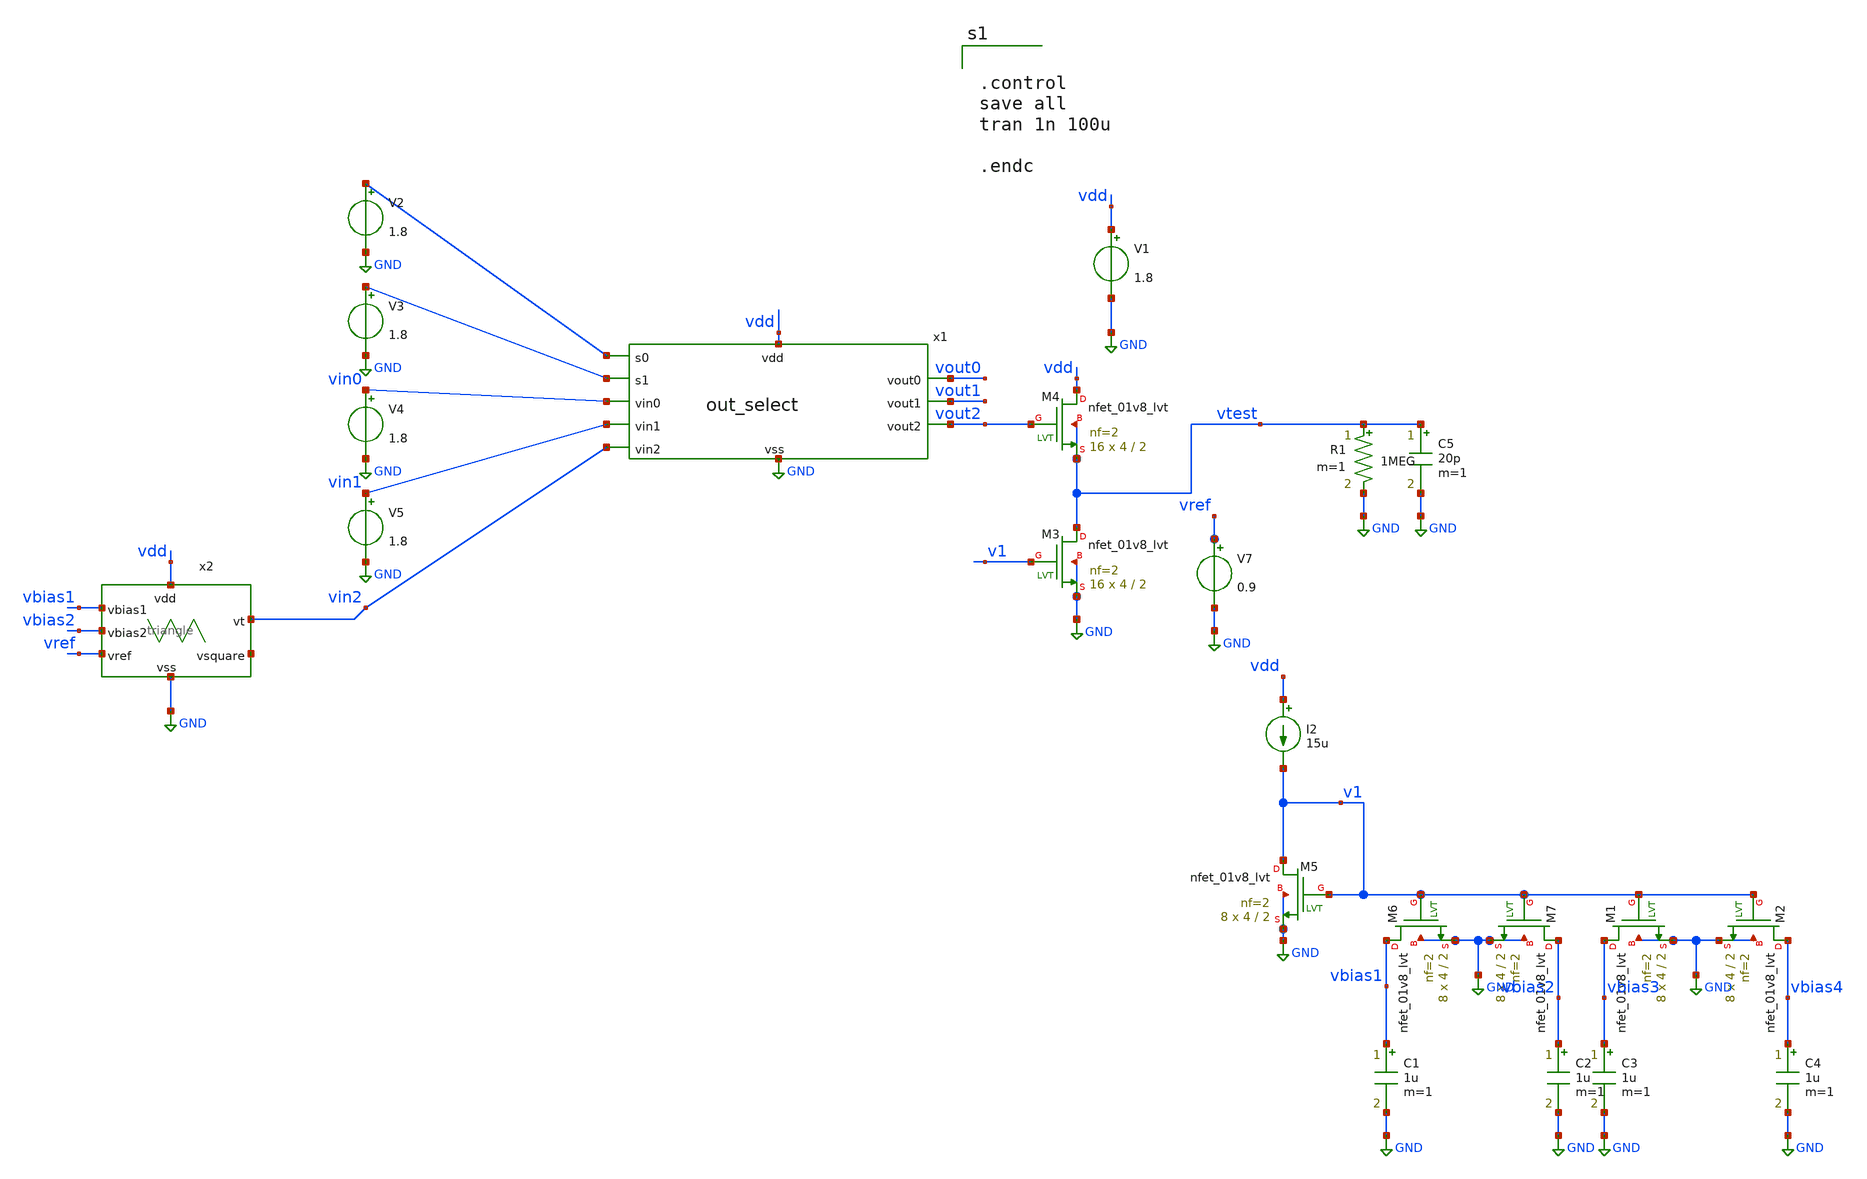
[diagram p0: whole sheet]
** sch_path: xschem/src/output_select/out_select_tb.sch
**.subckt out_select_tb
x1 vdd vin0 vout0 GND net1 vin1 vout1 net2 vin2 vout2 out_select
V1 vdd GND 1.8
V2 net1 GND 1.8
V3 net2 GND 1.8
V4 vin0 GND 1.8
V5 vin1 GND 1.8
V7 vref GND 0.9
I2 vdd v1 15u
XM5 v1 v1 GND GND sky130_fd_pr__nfet_01v8_lvt L=2 W=4 nf=2 ad='int((nf+1)/2) * W/nf * 0.29' as='int((nf+2)/2) * W/nf * 0.29'
+ pd='2*int((nf+1)/2) * (W/nf + 0.29)' ps='2*int((nf+2)/2) * (W/nf + 0.29)' nrd='0.29 / W' nrs='0.29 / W'
+ sa=0 sb=0 sd=0 mult=8 m=8
XM6 vbias1 v1 GND GND sky130_fd_pr__nfet_01v8_lvt L=2 W=4 nf=2 ad='int((nf+1)/2) * W/nf * 0.29' as='int((nf+2)/2) * W/nf * 0.29'
+ pd='2*int((nf+1)/2) * (W/nf + 0.29)' ps='2*int((nf+2)/2) * (W/nf + 0.29)' nrd='0.29 / W' nrs='0.29 / W'
+ sa=0 sb=0 sd=0 mult=8 m=8
XM7 vbias2 v1 GND GND sky130_fd_pr__nfet_01v8_lvt L=2 W=4 nf=2 ad='int((nf+1)/2) * W/nf * 0.29' as='int((nf+2)/2) * W/nf * 0.29'
+ pd='2*int((nf+1)/2) * (W/nf + 0.29)' ps='2*int((nf+2)/2) * (W/nf + 0.29)' nrd='0.29 / W' nrs='0.29 / W'
+ sa=0 sb=0 sd=0 mult=8 m=8
XM1 vbias3 v1 GND GND sky130_fd_pr__nfet_01v8_lvt L=2 W=4 nf=2 ad='int((nf+1)/2) * W/nf * 0.29' as='int((nf+2)/2) * W/nf * 0.29'
+ pd='2*int((nf+1)/2) * (W/nf + 0.29)' ps='2*int((nf+2)/2) * (W/nf + 0.29)' nrd='0.29 / W' nrs='0.29 / W'
+ sa=0 sb=0 sd=0 mult=8 m=8
XM2 vbias4 v1 GND GND sky130_fd_pr__nfet_01v8_lvt L=2 W=4 nf=2 ad='int((nf+1)/2) * W/nf * 0.29' as='int((nf+2)/2) * W/nf * 0.29'
+ pd='2*int((nf+1)/2) * (W/nf + 0.29)' ps='2*int((nf+2)/2) * (W/nf + 0.29)' nrd='0.29 / W' nrs='0.29 / W'
+ sa=0 sb=0 sd=0 mult=8 m=8
C1 vbias1 GND 1u m=1
C2 vbias2 GND 1u m=1
C3 vbias3 GND 1u m=1
C4 vbias4 GND 1u m=1
x2 vdd vbias1 vbias2 vref GND net3 vin2 triangle
C5 vtest GND 20p m=1
XM4 vdd vout2 vtest vtest sky130_fd_pr__nfet_01v8_lvt L=2 W=4 nf=2 ad='int((nf+1)/2) * W/nf * 0.29' as='int((nf+2)/2) * W/nf * 0.29'
+ pd='2*int((nf+1)/2) * (W/nf + 0.29)' ps='2*int((nf+2)/2) * (W/nf + 0.29)' nrd='0.29 / W' nrs='0.29 / W'
+ sa=0 sb=0 sd=0 mult=16 m=16
XM3 vtest v1 GND GND sky130_fd_pr__nfet_01v8_lvt L=2 W=4 nf=2 ad='int((nf+1)/2) * W/nf * 0.29' as='int((nf+2)/2) * W/nf * 0.29'
+ pd='2*int((nf+1)/2) * (W/nf + 0.29)' ps='2*int((nf+2)/2) * (W/nf + 0.29)' nrd='0.29 / W' nrs='0.29 / W'
+ sa=0 sb=0 sd=0 mult=16 m=16
R1 vtest GND 1MEG m=1
**** begin user architecture code

.include /home/eda/pdk/skywater-pdk/libraries/sky130_fd_pr_ngspice/latest/models/corners/tt.spice
.include /home/eda/magic/class_d_audio_amplifier/Class_D/Class_D_post.spice

* Resistor$::SKYWATER_MODELS/Capacitor
.include $::SKYWATER_MODELS/models/r+c/res_typical__cap_typical.spice
.include $::SKYWATER_MODELS/models/r+c/res_typical__cap_typical__lin.spice
* Special cells
.include $::SKYWATER_MODELS/models/corners/tt/specialized_cells.spice




.control
save all
tran 1n 100u

.endc




**** end user architecture code
**.ends

* expanding   symbol:  src/output_select/out_select.sym # of pins=10
** sym_path: xschem/src/output_select/out_select.sym
** sch_path: xschem/src/output_select/out_select.sch
.subckt out_select vdd vin0 vout0 vss s0 vin1 vout1 s1 vin2 vout2
*.ipin vin0
*.opin vout0
*.ipin vin1
*.opin vout1
*.ipin vin2
*.opin vout2
*.iopin vdd
*.iopin vss
*.ipin s0
*.ipin s1
x4 vdd sel0 net1 s1 vss nand
x5 vdd sel1 s0 net2 net4 nand
x6 vdd sel2 s0 s1 vss nand
x8 vdd s1 net2 vss inverter
x9 vdd s0 net1 vss inverter
x7 vdd sel2 net3 vss inverter
x10 vdd sel1 net7 net5 inverter
x11 vdd sel0 net6 vss inverter
XM1 vin0 net6 vout0 vout0 sky130_fd_pr__nfet_01v8 L=0.15 W=1 nf=1 ad='int((nf+1)/2) * W/nf * 0.29' as='int((nf+2)/2) * W/nf * 0.29'
+ pd='2*int((nf+1)/2) * (W/nf + 0.29)' ps='2*int((nf+2)/2) * (W/nf + 0.29)' nrd='0.29 / W' nrs='0.29 / W'
+ sa=0 sb=0 sd=0 mult=1 m=1
XM2 vin0 sel0 vout0 vout0 sky130_fd_pr__pfet_01v8 L=0.15 W=1 nf=1 ad='int((nf+1)/2) * W/nf * 0.29' as='int((nf+2)/2) * W/nf * 0.29'
+ pd='2*int((nf+1)/2) * (W/nf + 0.29)' ps='2*int((nf+2)/2) * (W/nf + 0.29)' nrd='0.29 / W' nrs='0.29 / W'
+ sa=0 sb=0 sd=0 mult=1 m=1
XM3 vin1 net7 vout1 vout1 sky130_fd_pr__nfet_01v8 L=0.15 W=1 nf=1 ad='int((nf+1)/2) * W/nf * 0.29' as='int((nf+2)/2) * W/nf * 0.29'
+ pd='2*int((nf+1)/2) * (W/nf + 0.29)' ps='2*int((nf+2)/2) * (W/nf + 0.29)' nrd='0.29 / W' nrs='0.29 / W'
+ sa=0 sb=0 sd=0 mult=1 m=1
XM4 vin1 sel1 vout1 vout1 sky130_fd_pr__pfet_01v8 L=0.15 W=1 nf=1 ad='int((nf+1)/2) * W/nf * 0.29' as='int((nf+2)/2) * W/nf * 0.29'
+ pd='2*int((nf+1)/2) * (W/nf + 0.29)' ps='2*int((nf+2)/2) * (W/nf + 0.29)' nrd='0.29 / W' nrs='0.29 / W'
+ sa=0 sb=0 sd=0 mult=1 m=1
XM5 vin2 net3 vout2 vout2 sky130_fd_pr__nfet_01v8 L=0.15 W=1 nf=1 ad='int((nf+1)/2) * W/nf * 0.29' as='int((nf+2)/2) * W/nf * 0.29'
+ pd='2*int((nf+1)/2) * (W/nf + 0.29)' ps='2*int((nf+2)/2) * (W/nf + 0.29)' nrd='0.29 / W' nrs='0.29 / W'
+ sa=0 sb=0 sd=0 mult=1 m=1
XM6 vin2 sel2 vout2 vout2 sky130_fd_pr__pfet_01v8 L=0.15 W=1 nf=1 ad='int((nf+1)/2) * W/nf * 0.29' as='int((nf+2)/2) * W/nf * 0.29'
+ pd='2*int((nf+1)/2) * (W/nf + 0.29)' ps='2*int((nf+2)/2) * (W/nf + 0.29)' nrd='0.29 / W' nrs='0.29 / W'
+ sa=0 sb=0 sd=0 mult=1 m=1
.ends


* expanding   symbol:  src/triangle/triangle.sym # of pins=7
** sym_path: xschem/src/triangle/triangle.sym
** sch_path: xschem/src/triangle/triangle.sch
.subckt triangle vdd vbias1 vbias2 vref vss vsquare vt
*.iopin vdd
*.ipin vbias1
*.opin vt
*.ipin vref
*.opin vsquare
*.iopin vss
*.ipin vbias2
XR3 vsquare vi vss sky130_fd_pr__res_xhigh_po L=32 mult=1 m=1
XR1 vt vcmp vss sky130_fd_pr__res_xhigh_po L=4 mult=1 m=1
XR2 vcmp vsquare vss sky130_fd_pr__res_xhigh_po L=9 mult=1 m=1
x1 vdd vref vi vbias1 vss vt OTA_tri
x2 vdd vcmp vref vbias2 vss vsquare OTA
XC1 vi vt sky130_fd_pr__cap_mim_m3_1 W=15 L=15 MF=8 m=8
.ends


* expanding   symbol:  src/nand/nand.sym # of pins=5
** sym_path: xschem/src/nand/nand.sym
** sch_path: xschem/src/nand/nand.sch
.subckt nand vdd out A B vss
*.ipin A
*.ipin B
*.opin out
*.iopin vdd
*.iopin vss
XM1 out A net1 vss sky130_fd_pr__nfet_01v8 L=0.15 W=2 nf=1 ad='int((nf+1)/2) * W/nf * 0.29' as='int((nf+2)/2) * W/nf * 0.29'
+ pd='2*int((nf+1)/2) * (W/nf + 0.29)' ps='2*int((nf+2)/2) * (W/nf + 0.29)' nrd='0.29 / W' nrs='0.29 / W'
+ sa=0 sb=0 sd=0 mult=1 m=1
XM2 out A vdd vdd sky130_fd_pr__pfet_01v8 L=0.15 W=2 nf=1 ad='int((nf+1)/2) * W/nf * 0.29' as='int((nf+2)/2) * W/nf * 0.29'
+ pd='2*int((nf+1)/2) * (W/nf + 0.29)' ps='2*int((nf+2)/2) * (W/nf + 0.29)' nrd='0.29 / W' nrs='0.29 / W'
+ sa=0 sb=0 sd=0 mult=1 m=1
XM3 net1 B vss vss sky130_fd_pr__nfet_01v8 L=0.15 W=2 nf=1 ad='int((nf+1)/2) * W/nf * 0.29' as='int((nf+2)/2) * W/nf * 0.29'
+ pd='2*int((nf+1)/2) * (W/nf + 0.29)' ps='2*int((nf+2)/2) * (W/nf + 0.29)' nrd='0.29 / W' nrs='0.29 / W'
+ sa=0 sb=0 sd=0 mult=1 m=1
XM4 out B vdd vdd sky130_fd_pr__pfet_01v8 L=0.15 W=2 nf=1 ad='int((nf+1)/2) * W/nf * 0.29' as='int((nf+2)/2) * W/nf * 0.29'
+ pd='2*int((nf+1)/2) * (W/nf + 0.29)' ps='2*int((nf+2)/2) * (W/nf + 0.29)' nrd='0.29 / W' nrs='0.29 / W'
+ sa=0 sb=0 sd=0 mult=1 m=1
.ends


* expanding   symbol:  src/inverter/inverter.sym # of pins=4
** sym_path: xschem/src/inverter/inverter.sym
** sch_path: xschem/src/inverter/inverter.sch
.subckt inverter vdd A B vss
*.iopin vdd
*.iopin vss
*.ipin A
*.opin B
XM3 B A vss vss sky130_fd_pr__nfet_01v8 L=0.15 W=1 nf=1 ad='int((nf+1)/2) * W/nf * 0.29' as='int((nf+2)/2) * W/nf * 0.29'
+ pd='2*int((nf+1)/2) * (W/nf + 0.29)' ps='2*int((nf+2)/2) * (W/nf + 0.29)' nrd='0.29 / W' nrs='0.29 / W'
+ sa=0 sb=0 sd=0 mult=1 m=1
XM1 B A vdd vdd sky130_fd_pr__pfet_01v8 L=0.15 W=2 nf=1 ad='int((nf+1)/2) * W/nf * 0.29' as='int((nf+2)/2) * W/nf * 0.29'
+ pd='2*int((nf+1)/2) * (W/nf + 0.29)' ps='2*int((nf+2)/2) * (W/nf + 0.29)' nrd='0.29 / W' nrs='0.29 / W'
+ sa=0 sb=0 sd=0 mult=1 m=1
.ends


* expanding   symbol:  src/OTA_tri/OTA_tri.sym # of pins=6
** sym_path: xschem/src/OTA_tri/OTA_tri.sym
** sch_path: xschem/src/OTA_tri/OTA_tri.sch
.subckt OTA_tri vdd vp vn vbias vss vout
*.ipin vp
*.ipin vn
*.ipin vbias
*.iopin vss
*.iopin vdd
*.opin vout
XM1 v1 vp vc vc sky130_fd_pr__pfet_01v8_lvt L=1 W=4 nf=1 ad='int((nf+1)/2) * W/nf * 0.29' as='int((nf+2)/2) * W/nf * 0.29'
+ pd='2*int((nf+1)/2) * (W/nf + 0.29)' ps='2*int((nf+2)/2) * (W/nf + 0.29)' nrd='0.29 / W' nrs='0.29 / W'
+ sa=0 sb=0 sd=0 mult=16 m=16
XM2 vf vn vc vc sky130_fd_pr__pfet_01v8_lvt L=1 W=4 nf=1 ad='int((nf+1)/2) * W/nf * 0.29' as='int((nf+2)/2) * W/nf * 0.29'
+ pd='2*int((nf+1)/2) * (W/nf + 0.29)' ps='2*int((nf+2)/2) * (W/nf + 0.29)' nrd='0.29 / W' nrs='0.29 / W'
+ sa=0 sb=0 sd=0 mult=16 m=16
XM3 vc vbias vdd vdd sky130_fd_pr__pfet_01v8_lvt L=1 W=2 nf=2 ad='int((nf+1)/2) * W/nf * 0.29' as='int((nf+2)/2) * W/nf * 0.29'
+ pd='2*int((nf+1)/2) * (W/nf + 0.29)' ps='2*int((nf+2)/2) * (W/nf + 0.29)' nrd='0.29 / W' nrs='0.29 / W'
+ sa=0 sb=0 sd=0 mult=24 m=24
XM4 v1 vf vss vss sky130_fd_pr__nfet_01v8_lvt L=1 W=1 nf=1 ad='int((nf+1)/2) * W/nf * 0.29' as='int((nf+2)/2) * W/nf * 0.29'
+ pd='2*int((nf+1)/2) * (W/nf + 0.29)' ps='2*int((nf+2)/2) * (W/nf + 0.29)' nrd='0.29 / W' nrs='0.29 / W'
+ sa=0 sb=0 sd=0 mult=16 m=16
XM5 vf vf vss vss sky130_fd_pr__nfet_01v8_lvt L=1 W=1 nf=1 ad='int((nf+1)/2) * W/nf * 0.29' as='int((nf+2)/2) * W/nf * 0.29'
+ pd='2*int((nf+1)/2) * (W/nf + 0.29)' ps='2*int((nf+2)/2) * (W/nf + 0.29)' nrd='0.29 / W' nrs='0.29 / W'
+ sa=0 sb=0 sd=0 mult=16 m=16
XM6 vbias vbias vdd vdd sky130_fd_pr__pfet_01v8_lvt L=1 W=2 nf=2 ad='int((nf+1)/2) * W/nf * 0.29' as='int((nf+2)/2) * W/nf * 0.29'
+ pd='2*int((nf+1)/2) * (W/nf + 0.29)' ps='2*int((nf+2)/2) * (W/nf + 0.29)' nrd='0.29 / W' nrs='0.29 / W'
+ sa=0 sb=0 sd=0 mult=24 m=24
XM7 vout vbias vdd vdd sky130_fd_pr__pfet_01v8_lvt L=1 W=2 nf=3 ad='int((nf+1)/2) * W/nf * 0.29' as='int((nf+2)/2) * W/nf * 0.29'
+ pd='2*int((nf+1)/2) * (W/nf + 0.29)' ps='2*int((nf+2)/2) * (W/nf + 0.29)' nrd='0.29 / W' nrs='0.29 / W'
+ sa=0 sb=0 sd=0 mult=48 m=48
XM8 vout v1 vss vss sky130_fd_pr__nfet_01v8_lvt L=1 W=1 nf=1 ad='int((nf+1)/2) * W/nf * 0.29' as='int((nf+2)/2) * W/nf * 0.29'
+ pd='2*int((nf+1)/2) * (W/nf + 0.29)' ps='2*int((nf+2)/2) * (W/nf + 0.29)' nrd='0.29 / W' nrs='0.29 / W'
+ sa=0 sb=0 sd=0 mult=64 m=64
XC1 net1 vout sky130_fd_pr__cap_mim_m3_1 W=27 L=18 MF=1 m=1
XR1 v1 net1 vss sky130_fd_pr__res_xhigh_po W=0.35 L=1.4 mult=1 m=1
.ends


* expanding   symbol:  src/OTA/OTA.sym # of pins=6
** sym_path: xschem/src/OTA/OTA.sym
** sch_path: xschem/src/OTA/OTA.sch
.subckt OTA vdd vp vn vbias vss vout
*.ipin vp
*.ipin vn
*.ipin vbias
*.iopin vss
*.iopin vdd
*.opin vout
XM1 v1 vp vc vc sky130_fd_pr__pfet_01v8_lvt L=1 W=4 nf=1 ad='int((nf+1)/2) * W/nf * 0.29' as='int((nf+2)/2) * W/nf * 0.29'
+ pd='2*int((nf+1)/2) * (W/nf + 0.29)' ps='2*int((nf+2)/2) * (W/nf + 0.29)' nrd='0.29 / W' nrs='0.29 / W'
+ sa=0 sb=0 sd=0 mult=16 m=16
XM2 vf vn vc vc sky130_fd_pr__pfet_01v8_lvt L=1 W=4 nf=1 ad='int((nf+1)/2) * W/nf * 0.29' as='int((nf+2)/2) * W/nf * 0.29'
+ pd='2*int((nf+1)/2) * (W/nf + 0.29)' ps='2*int((nf+2)/2) * (W/nf + 0.29)' nrd='0.29 / W' nrs='0.29 / W'
+ sa=0 sb=0 sd=0 mult=16 m=16
XM3 vc vbias vdd vdd sky130_fd_pr__pfet_01v8_lvt L=1 W=2 nf=2 ad='int((nf+1)/2) * W/nf * 0.29' as='int((nf+2)/2) * W/nf * 0.29'
+ pd='2*int((nf+1)/2) * (W/nf + 0.29)' ps='2*int((nf+2)/2) * (W/nf + 0.29)' nrd='0.29 / W' nrs='0.29 / W'
+ sa=0 sb=0 sd=0 mult=24 m=24
XM4 v1 vf vss vss sky130_fd_pr__nfet_01v8_lvt L=1 W=1 nf=1 ad='int((nf+1)/2) * W/nf * 0.29' as='int((nf+2)/2) * W/nf * 0.29'
+ pd='2*int((nf+1)/2) * (W/nf + 0.29)' ps='2*int((nf+2)/2) * (W/nf + 0.29)' nrd='0.29 / W' nrs='0.29 / W'
+ sa=0 sb=0 sd=0 mult=16 m=16
XM5 vf vf vss vss sky130_fd_pr__nfet_01v8_lvt L=1 W=1 nf=1 ad='int((nf+1)/2) * W/nf * 0.29' as='int((nf+2)/2) * W/nf * 0.29'
+ pd='2*int((nf+1)/2) * (W/nf + 0.29)' ps='2*int((nf+2)/2) * (W/nf + 0.29)' nrd='0.29 / W' nrs='0.29 / W'
+ sa=0 sb=0 sd=0 mult=16 m=16
XM6 vbias vbias vdd vdd sky130_fd_pr__pfet_01v8_lvt L=1 W=2 nf=2 ad='int((nf+1)/2) * W/nf * 0.29' as='int((nf+2)/2) * W/nf * 0.29'
+ pd='2*int((nf+1)/2) * (W/nf + 0.29)' ps='2*int((nf+2)/2) * (W/nf + 0.29)' nrd='0.29 / W' nrs='0.29 / W'
+ sa=0 sb=0 sd=0 mult=24 m=24
XM7 vout vbias vdd vdd sky130_fd_pr__pfet_01v8_lvt L=1 W=2 nf=2 ad='int((nf+1)/2) * W/nf * 0.29' as='int((nf+2)/2) * W/nf * 0.29'
+ pd='2*int((nf+1)/2) * (W/nf + 0.29)' ps='2*int((nf+2)/2) * (W/nf + 0.29)' nrd='0.29 / W' nrs='0.29 / W'
+ sa=0 sb=0 sd=0 mult=48 m=48
XM8 vout v1 vss vss sky130_fd_pr__nfet_01v8_lvt L=1 W=1 nf=1 ad='int((nf+1)/2) * W/nf * 0.29' as='int((nf+2)/2) * W/nf * 0.29'
+ pd='2*int((nf+1)/2) * (W/nf + 0.29)' ps='2*int((nf+2)/2) * (W/nf + 0.29)' nrd='0.29 / W' nrs='0.29 / W'
+ sa=0 sb=0 sd=0 mult=64 m=64
XR1 v1 net1 vss sky130_fd_pr__res_xhigh_po W=0.35 L=0.5 mult=1 m=1
XC2 net1 vout sky130_fd_pr__cap_mim_m3_1 W=14 L=14 MF=1 m=1
.ends

.GLOBAL GND
.end
